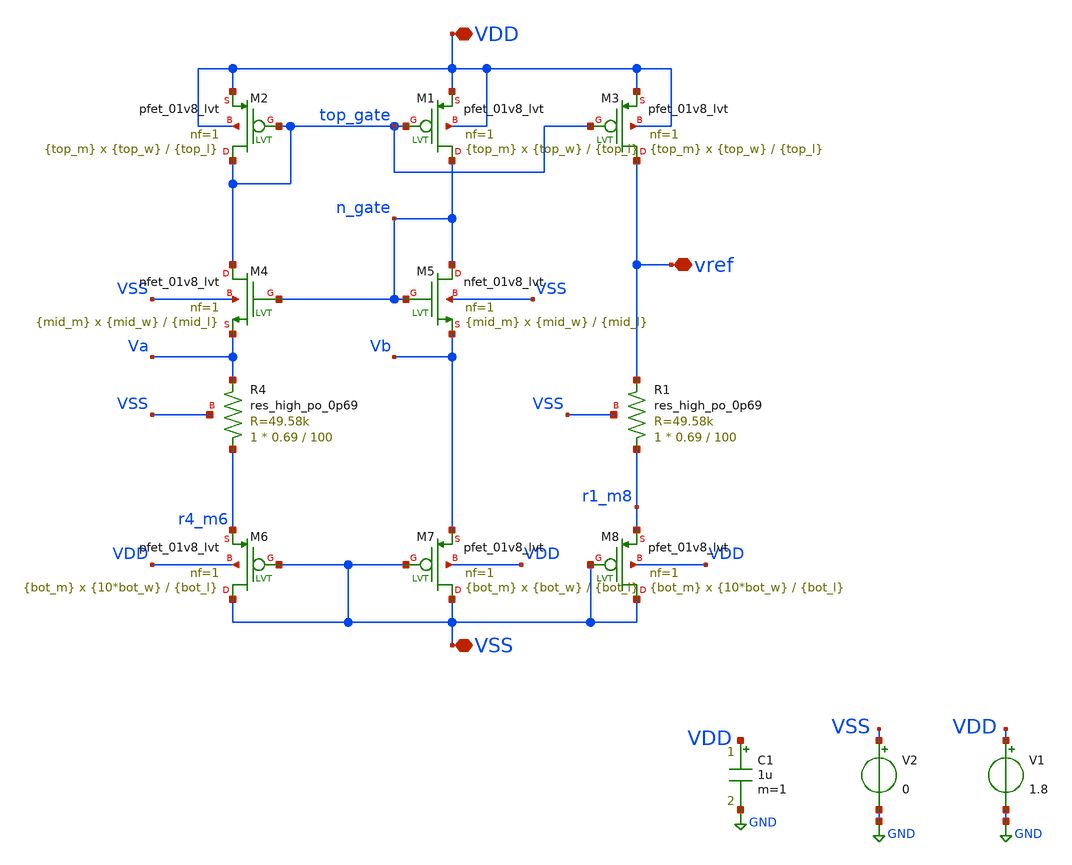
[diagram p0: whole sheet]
** sch_path: xschem/bandgap-op.sch
**.subckt bandgap-op VSS VDD vref
*.iopin VSS
*.iopin VDD
*.iopin vref
XR4 r4_m6 Va VSS sky130_fd_pr__res_high_po_0p69 L=100 mult=1 m=1
XR1 r1_m8 vref VSS sky130_fd_pr__res_high_po_0p69 L=100 mult=1 m=1
V1 VDD GND 1.8
V2 VSS GND 0
C1 VDD GND 1u m=1
XM5 n_gate n_gate Vb VSS sky130_fd_pr__nfet_01v8_lvt L={mid_l} W={mid_w} nf=1 ad='int((nf+1)/2) * W/nf * 0.29'
+ as='int((nf+2)/2) * W/nf * 0.29' pd='2*int((nf+1)/2) * (W/nf + 0.29)' ps='2*int((nf+2)/2) * (W/nf + 0.29)'
+ nrd='0.29 / W' nrs='0.29 / W' sa=0 sb=0 sd=0 mult={mid_m} m={mid_m}
XM3 vref top_gate VDD VDD sky130_fd_pr__pfet_01v8_lvt L={top_l} W={top_w} nf=1 ad='int((nf+1)/2) * W/nf * 0.29'
+ as='int((nf+2)/2) * W/nf * 0.29' pd='2*int((nf+1)/2) * (W/nf + 0.29)' ps='2*int((nf+2)/2) * (W/nf + 0.29)'
+ nrd='0.29 / W' nrs='0.29 / W' sa=0 sb=0 sd=0 mult={top_m} m={top_m}
XM1 n_gate top_gate VDD VDD sky130_fd_pr__pfet_01v8_lvt L={top_l} W={top_w} nf=1 ad='int((nf+1)/2) * W/nf * 0.29'
+ as='int((nf+2)/2) * W/nf * 0.29' pd='2*int((nf+1)/2) * (W/nf + 0.29)' ps='2*int((nf+2)/2) * (W/nf + 0.29)'
+ nrd='0.29 / W' nrs='0.29 / W' sa=0 sb=0 sd=0 mult={top_m} m={top_m}
XM2 top_gate top_gate VDD VDD sky130_fd_pr__pfet_01v8_lvt L={top_l} W={top_w} nf=1 ad='int((nf+1)/2) * W/nf * 0.29'
+ as='int((nf+2)/2) * W/nf * 0.29' pd='2*int((nf+1)/2) * (W/nf + 0.29)' ps='2*int((nf+2)/2) * (W/nf + 0.29)'
+ nrd='0.29 / W' nrs='0.29 / W' sa=0 sb=0 sd=0 mult={top_m} m={top_m}
XM4 top_gate n_gate Va VSS sky130_fd_pr__nfet_01v8_lvt L={mid_l} W={mid_w} nf=1 ad='int((nf+1)/2) * W/nf * 0.29'
+ as='int((nf+2)/2) * W/nf * 0.29' pd='2*int((nf+1)/2) * (W/nf + 0.29)' ps='2*int((nf+2)/2) * (W/nf + 0.29)'
+ nrd='0.29 / W' nrs='0.29 / W' sa=0 sb=0 sd=0 mult={mid_m} m={mid_m}
XM6 VSS VSS r4_m6 VDD sky130_fd_pr__pfet_01v8_lvt L={bot_l} W={10*bot_w} nf=1 ad='int((nf+1)/2) * W/nf * 0.29'
+ as='int((nf+2)/2) * W/nf * 0.29' pd='2*int((nf+1)/2) * (W/nf + 0.29)' ps='2*int((nf+2)/2) * (W/nf + 0.29)'
+ nrd='0.29 / W' nrs='0.29 / W' sa=0 sb=0 sd=0 mult={bot_m} m={bot_m}
XM8 VSS VSS r1_m8 VDD sky130_fd_pr__pfet_01v8_lvt L={bot_l} W={10*bot_w} nf=1 ad='int((nf+1)/2) * W/nf * 0.29'
+ as='int((nf+2)/2) * W/nf * 0.29' pd='2*int((nf+1)/2) * (W/nf + 0.29)' ps='2*int((nf+2)/2) * (W/nf + 0.29)'
+ nrd='0.29 / W' nrs='0.29 / W' sa=0 sb=0 sd=0 mult={bot_m} m={bot_m}
XM7 VSS VSS Vb VDD sky130_fd_pr__pfet_01v8_lvt L={bot_l} W={bot_w} nf=1 ad='int((nf+1)/2) * W/nf * 0.29'
+ as='int((nf+2)/2) * W/nf * 0.29' pd='2*int((nf+1)/2) * (W/nf + 0.29)' ps='2*int((nf+2)/2) * (W/nf + 0.29)'
+ nrd='0.29 / W' nrs='0.29 / W' sa=0 sb=0 sd=0 mult={bot_m} m={bot_m}
**** begin user architecture code

** opencircuitdesign pdks install
.lib $::SKYWATER_MODELS/sky130.lib.spice tt





.param top_l = 10
.param top_w = 10
.param top_m = 10

.param mid_l = 4
.param mid_w = 10
.param mid_m = 1

.param bot_l = 10
.param bot_w = 10
.param bot_m = 10

.control
op
write bandgap-op.raw
set appendwrite
reset

dc v1 1.3 2 0.05
write bandgap-op.raw
reset

dc temp 10 100 4
write bandgap-op.raw

.endc



**** end user architecture code
**.ends
.GLOBAL GND
.end
